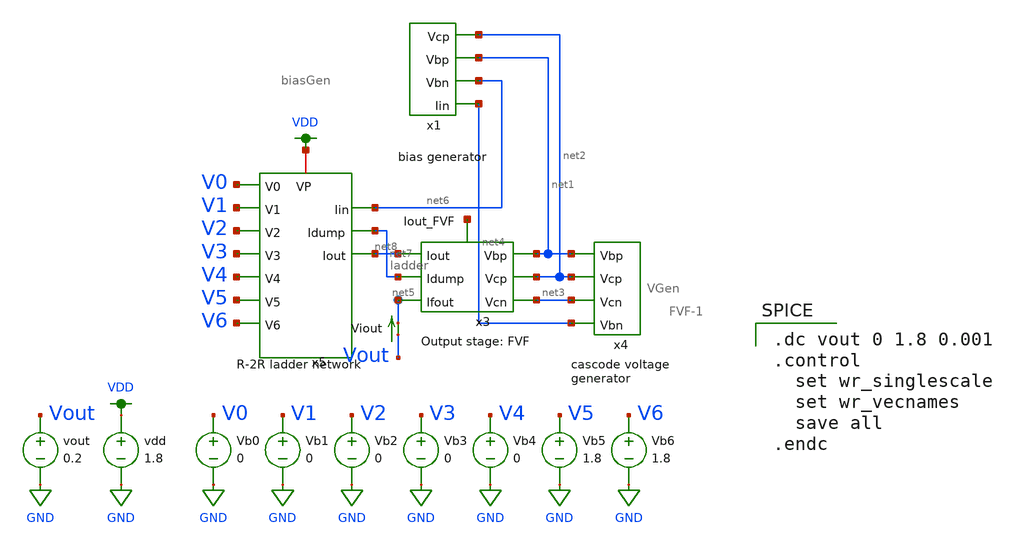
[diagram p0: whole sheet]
** sch_path: xschem/mp4_dac_simulation_supply_sweep_cascoded.sch
**.subckt mp4_dac_simulation_supply_sweep_cascoded
Vb1 V1 GND 0
Vb2 V2 GND 0
Vb3 V3 GND 0
Vb4 V4 GND 0
Vb5 V5 GND 1.8
Vb6 V6 GND 1.8
Vb0 V0 GND 0
x3 net1 net2 net8 net3 net5 net7 net9 FVF-1
x4 net1 net3 net2 net4 VGen
vdd VDD GND 1.8
vout Vout GND 0.2
Viout Vout net5 0
.save i(viout)
x5 V0 VDD net7 net8 net6 V1 V2 V3 V4 V5 V6 ladder
x1 net1 net4 net6 net2 biasGen
**** begin user architecture code

.option wnflag=1
.param MC_SWITCH=0.0
.lib ~/skywater/skywater-pdk/libraries/sky130_fd_pr_ngspice/latest/models/sky130.lib.spice tt


.dc vout 0 1.8 0.001
.control
  set wr_singlescale
  set wr_vecnames
  save all
.endc

**** end user architecture code
**.ends
.GLOBAL GND
.GLOBAL VDD
.end
